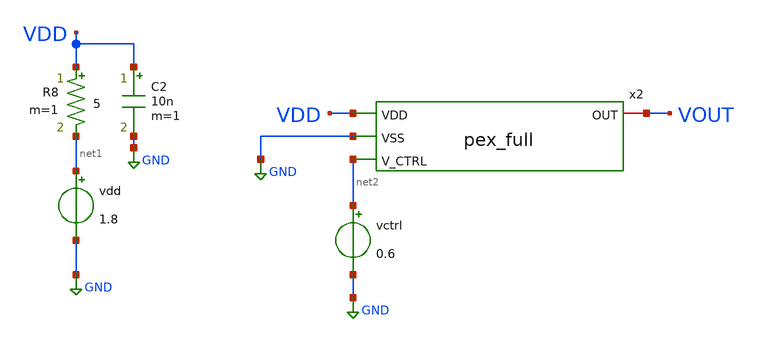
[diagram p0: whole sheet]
** sch_path: schem/mc_full_tb.sch
**.subckt mc_full_tb
vdd net1 GND 1.8
C2 VDD GND 10n m=1
R8 VDD net1 5 m=1
vctrl net2 GND 0.6
x2 VDD GND VOUT net2 vco_pex
**** begin user architecture code


.include /home/zhixuan/projects/fyp_vco/magic/full/vco_pex.spice
.lib /usr/local/share/pdk/sky130A/libs.tech/ngspice/sky130.lib.spice tt

.param mc_mm_switch=1
.param mc_pr_switch=1

.tran 0.1n 2u
.save all

.control
    run

    meas tran t11 when VOUT=0.9 rise=2
    meas tran t21 when VOUT=0.9 rise=3

    if t11 > 0 and t21 > t11
        let period1 = t21 - t11
        let freq1 = 1 / period1

        meas tran idd1 avg i(vdd) from=t11 to=2u
        let idd1 = abs(idd1)

        echo RESULT freq1 $&freq1 period1 $&period1 idd1 $&idd1
    else
        echo RESULT FAILED
    end

.endc
.end


**** end user architecture code
**.ends
.GLOBAL GND
.end
